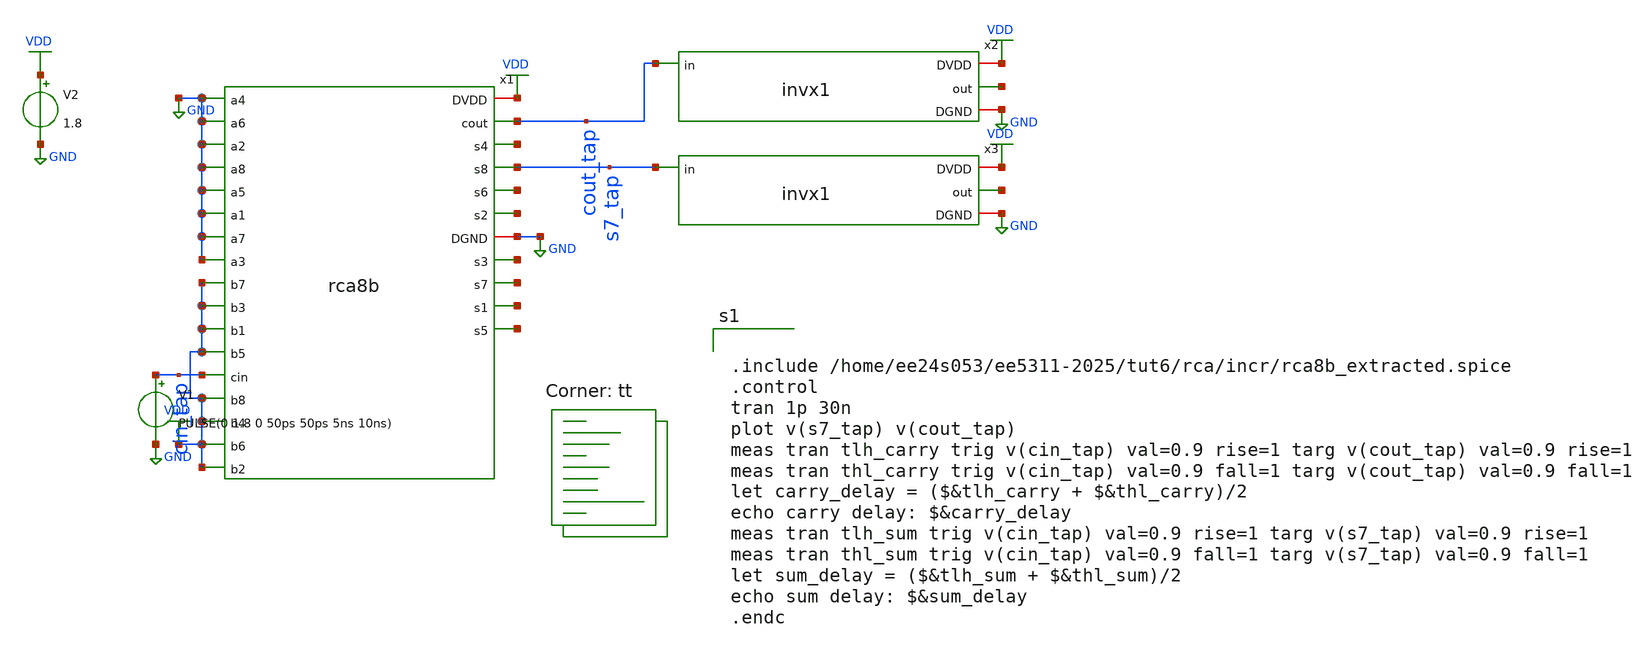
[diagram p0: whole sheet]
** sch_path: tut6/rca/incr/rca8b_tb.sch
**.subckt rca8b_tb
x1 GND GND GND GND GND GND GND GND VDD VDD VDD VDD VDD cout_tap net1 s7_tap net2 net3 cin_tap GND
+ net4 net5 net6 net7 VDD VDD VDD VDD rca8b
V1 cin_tap GND PULSE(0 1.8 0 50ps 50ps 5ns 10ns)
V2 VDD GND 1.8
x2 VDD cout_tap net8 GND invx1
x3 VDD s7_tap net9 GND invx1
**** begin user architecture code
.lib $::SKYWATER_MODELS/sky130.lib.spice tt


.include /home/ee24s053/ee5311-2025/tut6/rca/incr/rca8b_extracted.spice
.control
tran 1p 30n
plot v(s7_tap) v(cout_tap)
meas tran tlh_carry trig v(cin_tap) val=0.9 rise=1 targ v(cout_tap) val=0.9 rise=1
meas tran thl_carry trig v(cin_tap) val=0.9 fall=1 targ v(cout_tap) val=0.9 fall=1
let carry_delay = ($&tlh_carry + $&thl_carry)/2
echo carry delay: $&carry_delay
meas tran tlh_sum trig v(cin_tap) val=0.9 rise=1 targ v(s7_tap) val=0.9 rise=1
meas tran thl_sum trig v(cin_tap) val=0.9 fall=1 targ v(s7_tap) val=0.9 fall=1
let sum_delay = ($&tlh_sum + $&thl_sum)/2
echo sum delay: $&sum_delay
.endc

**** end user architecture code
**.ends
.GLOBAL VDD
.GLOBAL GND
.end
